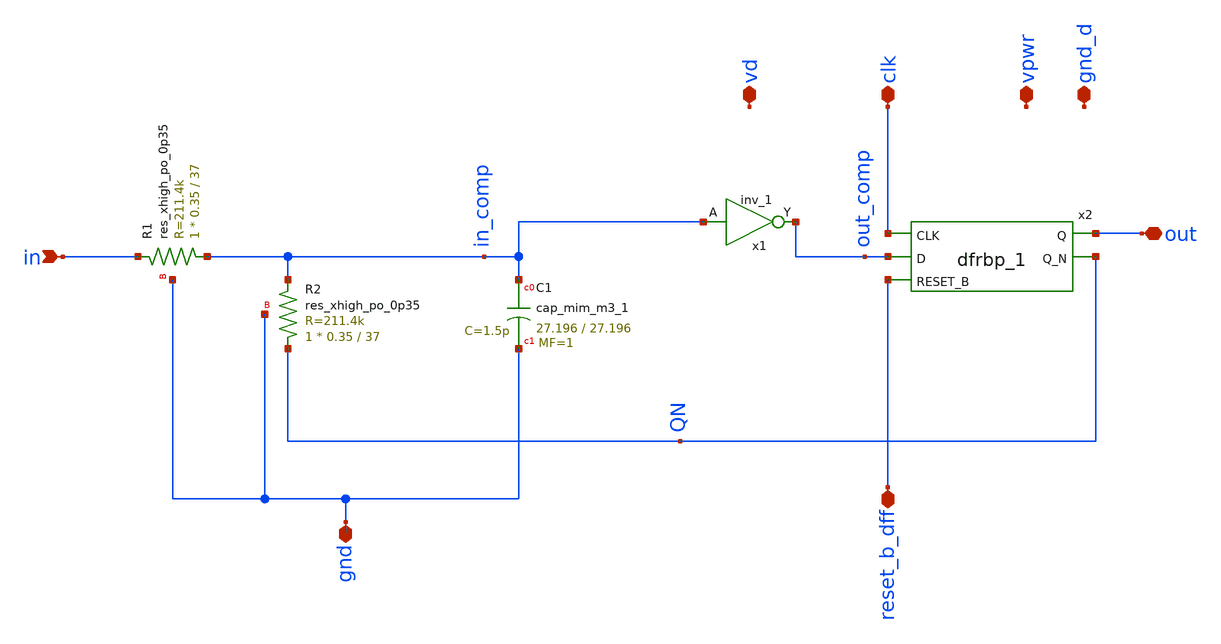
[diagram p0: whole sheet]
** sch_path: sigma-delta_modulator/xschem/sigma-delta.sch
* Copyright 2020 Stefan Frederik Schippers
* Licensed under the Apache License, Version 2.0 (the "License");
* you may not use this file except in compliance with the License.
* You may obtain a copy of the License at
* https://www.apache.org/licenses/LICENSE-2.0
* Unless required by applicable law or agreed to in writing, software
* distributed under the License is distributed on an "AS IS" BASIS,
* WITHOUT WARRANTIES OR CONDITIONS OF ANY KIND, either express or implied.
* See the License for the specific language governing permissions and
* limitations under the License.
**.subckt sigma-delta in gnd clk out reset_b_dff vpwr gnd_d vd
*.ipin in
*.iopin gnd
*.iopin clk
*.iopin out
*.iopin reset_b_dff
*.iopin vpwr
*.iopin gnd_d
*.iopin vd
XC1 in_comp gnd sky130_fd_pr__cap_mim_m3_1 W=27.196 L=27.196 MF=1 m=1
XR2 QN in_comp gnd sky130_fd_pr__res_xhigh_po_0p35 L=37 mult=1 m=1
x2 clk out_comp reset_b_dff gnd_d gnd_d vpwr vpwr out QN sky130_fd_sc_hd__dfrbp_1
XR1 in_comp in gnd sky130_fd_pr__res_xhigh_po_0p35 L=37 mult=1 m=1
x1 in_comp gnd_d gnd_d vpwr VPWR out_comp sky130_fd_sc_hd__inv_1
**** begin user architecture code




**** end user architecture code
**.ends
.end
